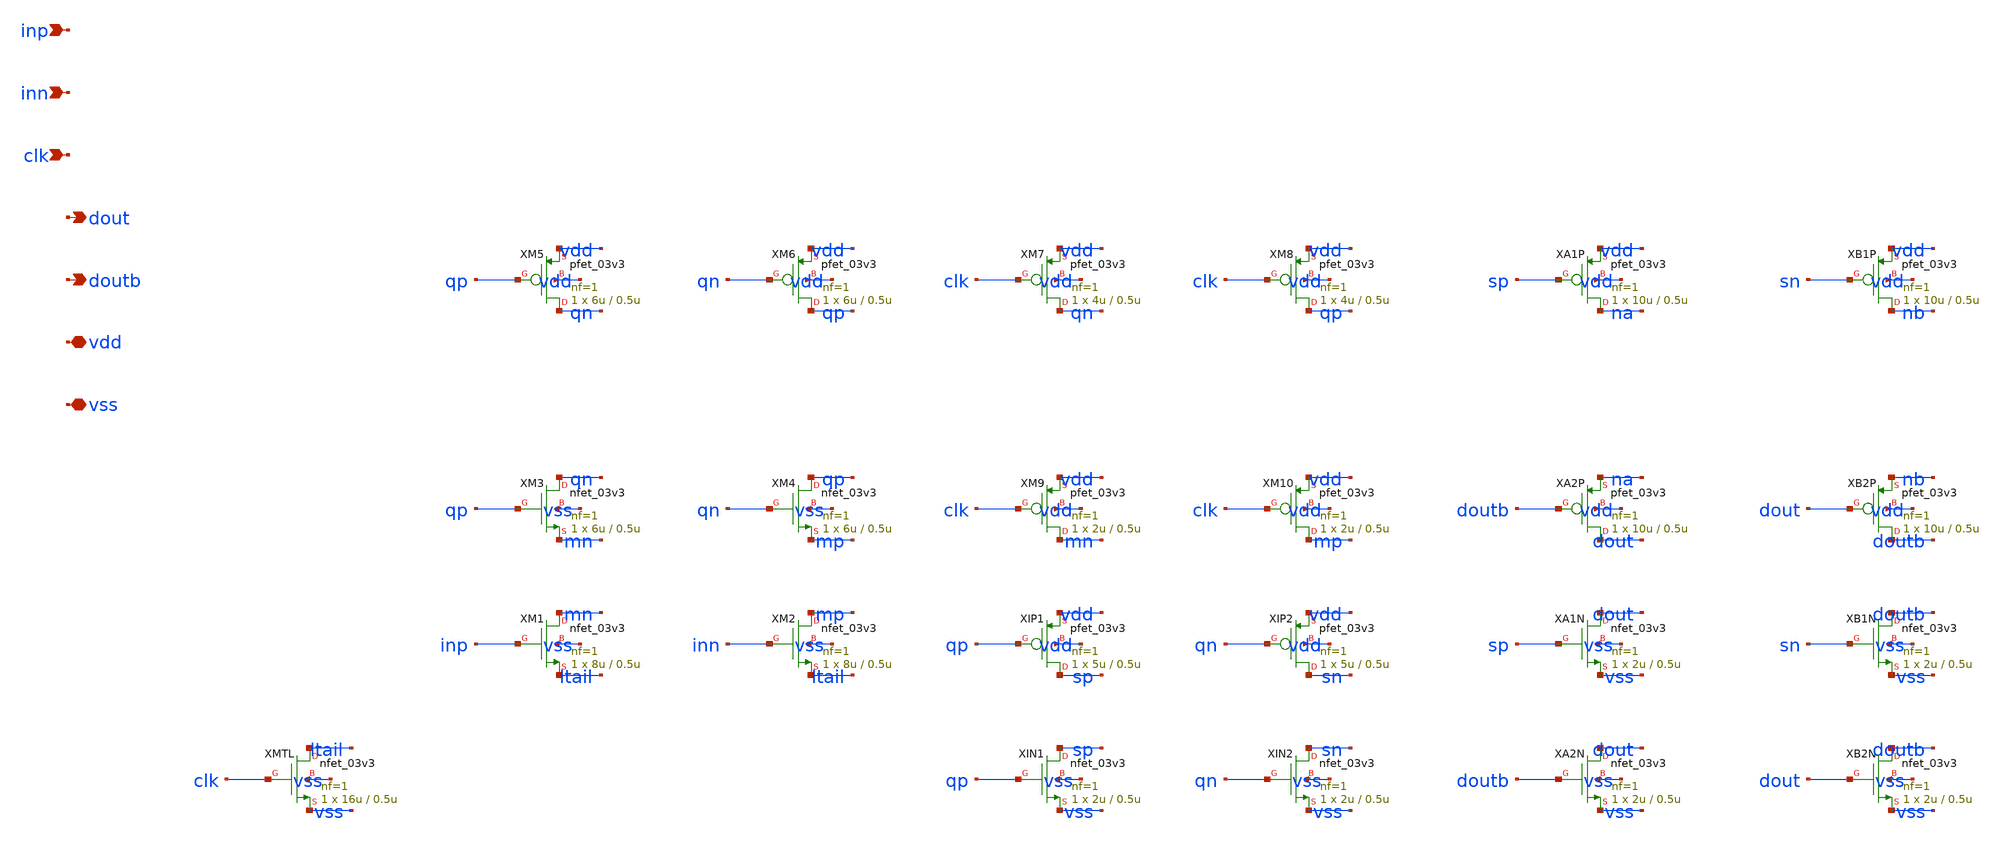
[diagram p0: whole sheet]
** sch_path: design/comparator_dut_latch.sch
**.subckt comparator_dut_latch inp inn clk dout doutb vdd vss
*.ipin inp
*.ipin inn
*.ipin clk
*.opin dout
*.opin doutb
*.iopin vdd
*.iopin vss
XMTL ltail clk vss vss nfet_03v3 L=0.5u W=16u nf=1 ad='int((nf+1)/2) * W/nf * 0.18u' as='int((nf+2)/2) * W/nf * 0.18u'
+ pd='2*int((nf+1)/2) * (W/nf + 0.18u)' ps='2*int((nf+2)/2) * (W/nf + 0.18u)' nrd='0.18u / W' nrs='0.18u / W'
+ sa=0 sb=0 sd=0 m=1
XM1 mn inp ltail vss nfet_03v3 L=0.5u W=8u nf=1 ad='int((nf+1)/2) * W/nf * 0.18u' as='int((nf+2)/2) * W/nf * 0.18u'
+ pd='2*int((nf+1)/2) * (W/nf + 0.18u)' ps='2*int((nf+2)/2) * (W/nf + 0.18u)' nrd='0.18u / W' nrs='0.18u / W'
+ sa=0 sb=0 sd=0 m=1
XM2 mp inn ltail vss nfet_03v3 L=0.5u W=8u nf=1 ad='int((nf+1)/2) * W/nf * 0.18u' as='int((nf+2)/2) * W/nf * 0.18u'
+ pd='2*int((nf+1)/2) * (W/nf + 0.18u)' ps='2*int((nf+2)/2) * (W/nf + 0.18u)' nrd='0.18u / W' nrs='0.18u / W'
+ sa=0 sb=0 sd=0 m=1
XM3 qn qp mn vss nfet_03v3 L=0.5u W=6u nf=1 ad='int((nf+1)/2) * W/nf * 0.18u' as='int((nf+2)/2) * W/nf * 0.18u'
+ pd='2*int((nf+1)/2) * (W/nf + 0.18u)' ps='2*int((nf+2)/2) * (W/nf + 0.18u)' nrd='0.18u / W' nrs='0.18u / W'
+ sa=0 sb=0 sd=0 m=1
XM4 qp qn mp vss nfet_03v3 L=0.5u W=6u nf=1 ad='int((nf+1)/2) * W/nf * 0.18u' as='int((nf+2)/2) * W/nf * 0.18u'
+ pd='2*int((nf+1)/2) * (W/nf + 0.18u)' ps='2*int((nf+2)/2) * (W/nf + 0.18u)' nrd='0.18u / W' nrs='0.18u / W'
+ sa=0 sb=0 sd=0 m=1
XM5 qn qp vdd vdd pfet_03v3 L=0.5u W=6u nf=1 ad='int((nf+1)/2) * W/nf * 0.18u' as='int((nf+2)/2) * W/nf * 0.18u'
+ pd='2*int((nf+1)/2) * (W/nf + 0.18u)' ps='2*int((nf+2)/2) * (W/nf + 0.18u)' nrd='0.18u / W' nrs='0.18u / W'
+ sa=0 sb=0 sd=0 m=1
XM6 qp qn vdd vdd pfet_03v3 L=0.5u W=6u nf=1 ad='int((nf+1)/2) * W/nf * 0.18u' as='int((nf+2)/2) * W/nf * 0.18u'
+ pd='2*int((nf+1)/2) * (W/nf + 0.18u)' ps='2*int((nf+2)/2) * (W/nf + 0.18u)' nrd='0.18u / W' nrs='0.18u / W'
+ sa=0 sb=0 sd=0 m=1
XM7 qn clk vdd vdd pfet_03v3 L=0.5u W=4u nf=1 ad='int((nf+1)/2) * W/nf * 0.18u' as='int((nf+2)/2) * W/nf * 0.18u'
+ pd='2*int((nf+1)/2) * (W/nf + 0.18u)' ps='2*int((nf+2)/2) * (W/nf + 0.18u)' nrd='0.18u / W' nrs='0.18u / W'
+ sa=0 sb=0 sd=0 m=1
XM8 qp clk vdd vdd pfet_03v3 L=0.5u W=4u nf=1 ad='int((nf+1)/2) * W/nf * 0.18u' as='int((nf+2)/2) * W/nf * 0.18u'
+ pd='2*int((nf+1)/2) * (W/nf + 0.18u)' ps='2*int((nf+2)/2) * (W/nf + 0.18u)' nrd='0.18u / W' nrs='0.18u / W'
+ sa=0 sb=0 sd=0 m=1
XM9 mn clk vdd vdd pfet_03v3 L=0.5u W=2u nf=1 ad='int((nf+1)/2) * W/nf * 0.18u' as='int((nf+2)/2) * W/nf * 0.18u'
+ pd='2*int((nf+1)/2) * (W/nf + 0.18u)' ps='2*int((nf+2)/2) * (W/nf + 0.18u)' nrd='0.18u / W' nrs='0.18u / W'
+ sa=0 sb=0 sd=0 m=1
XM10 mp clk vdd vdd pfet_03v3 L=0.5u W=2u nf=1 ad='int((nf+1)/2) * W/nf * 0.18u' as='int((nf+2)/2) * W/nf * 0.18u'
+ pd='2*int((nf+1)/2) * (W/nf + 0.18u)' ps='2*int((nf+2)/2) * (W/nf + 0.18u)' nrd='0.18u / W' nrs='0.18u / W'
+ sa=0 sb=0 sd=0 m=1
XIP1 sp qp vdd vdd pfet_03v3 L=0.5u W=5u nf=1 ad='int((nf+1)/2) * W/nf * 0.18u' as='int((nf+2)/2) * W/nf * 0.18u'
+ pd='2*int((nf+1)/2) * (W/nf + 0.18u)' ps='2*int((nf+2)/2) * (W/nf + 0.18u)' nrd='0.18u / W' nrs='0.18u / W'
+ sa=0 sb=0 sd=0 m=1
XIN1 sp qp vss vss nfet_03v3 L=0.5u W=2u nf=1 ad='int((nf+1)/2) * W/nf * 0.18u' as='int((nf+2)/2) * W/nf * 0.18u'
+ pd='2*int((nf+1)/2) * (W/nf + 0.18u)' ps='2*int((nf+2)/2) * (W/nf + 0.18u)' nrd='0.18u / W' nrs='0.18u / W'
+ sa=0 sb=0 sd=0 m=1
XIP2 sn qn vdd vdd pfet_03v3 L=0.5u W=5u nf=1 ad='int((nf+1)/2) * W/nf * 0.18u' as='int((nf+2)/2) * W/nf * 0.18u'
+ pd='2*int((nf+1)/2) * (W/nf + 0.18u)' ps='2*int((nf+2)/2) * (W/nf + 0.18u)' nrd='0.18u / W' nrs='0.18u / W'
+ sa=0 sb=0 sd=0 m=1
XIN2 sn qn vss vss nfet_03v3 L=0.5u W=2u nf=1 ad='int((nf+1)/2) * W/nf * 0.18u' as='int((nf+2)/2) * W/nf * 0.18u'
+ pd='2*int((nf+1)/2) * (W/nf + 0.18u)' ps='2*int((nf+2)/2) * (W/nf + 0.18u)' nrd='0.18u / W' nrs='0.18u / W'
+ sa=0 sb=0 sd=0 m=1
XA1P na sp vdd vdd pfet_03v3 L=0.5u W=10u nf=1 ad='int((nf+1)/2) * W/nf * 0.18u' as='int((nf+2)/2) * W/nf * 0.18u'
+ pd='2*int((nf+1)/2) * (W/nf + 0.18u)' ps='2*int((nf+2)/2) * (W/nf + 0.18u)' nrd='0.18u / W' nrs='0.18u / W'
+ sa=0 sb=0 sd=0 m=1
XA2P dout doutb na vdd pfet_03v3 L=0.5u W=10u nf=1 ad='int((nf+1)/2) * W/nf * 0.18u' as='int((nf+2)/2) * W/nf * 0.18u'
+ pd='2*int((nf+1)/2) * (W/nf + 0.18u)' ps='2*int((nf+2)/2) * (W/nf + 0.18u)' nrd='0.18u / W' nrs='0.18u / W'
+ sa=0 sb=0 sd=0 m=1
XA1N dout sp vss vss nfet_03v3 L=0.5u W=2u nf=1 ad='int((nf+1)/2) * W/nf * 0.18u' as='int((nf+2)/2) * W/nf * 0.18u'
+ pd='2*int((nf+1)/2) * (W/nf + 0.18u)' ps='2*int((nf+2)/2) * (W/nf + 0.18u)' nrd='0.18u / W' nrs='0.18u / W'
+ sa=0 sb=0 sd=0 m=1
XA2N dout doutb vss vss nfet_03v3 L=0.5u W=2u nf=1 ad='int((nf+1)/2) * W/nf * 0.18u' as='int((nf+2)/2) * W/nf * 0.18u'
+ pd='2*int((nf+1)/2) * (W/nf + 0.18u)' ps='2*int((nf+2)/2) * (W/nf + 0.18u)' nrd='0.18u / W' nrs='0.18u / W'
+ sa=0 sb=0 sd=0 m=1
XB1P nb sn vdd vdd pfet_03v3 L=0.5u W=10u nf=1 ad='int((nf+1)/2) * W/nf * 0.18u' as='int((nf+2)/2) * W/nf * 0.18u'
+ pd='2*int((nf+1)/2) * (W/nf + 0.18u)' ps='2*int((nf+2)/2) * (W/nf + 0.18u)' nrd='0.18u / W' nrs='0.18u / W'
+ sa=0 sb=0 sd=0 m=1
XB2P doutb dout nb vdd pfet_03v3 L=0.5u W=10u nf=1 ad='int((nf+1)/2) * W/nf * 0.18u' as='int((nf+2)/2) * W/nf * 0.18u'
+ pd='2*int((nf+1)/2) * (W/nf + 0.18u)' ps='2*int((nf+2)/2) * (W/nf + 0.18u)' nrd='0.18u / W' nrs='0.18u / W'
+ sa=0 sb=0 sd=0 m=1
XB1N doutb sn vss vss nfet_03v3 L=0.5u W=2u nf=1 ad='int((nf+1)/2) * W/nf * 0.18u' as='int((nf+2)/2) * W/nf * 0.18u'
+ pd='2*int((nf+1)/2) * (W/nf + 0.18u)' ps='2*int((nf+2)/2) * (W/nf + 0.18u)' nrd='0.18u / W' nrs='0.18u / W'
+ sa=0 sb=0 sd=0 m=1
XB2N doutb dout vss vss nfet_03v3 L=0.5u W=2u nf=1 ad='int((nf+1)/2) * W/nf * 0.18u' as='int((nf+2)/2) * W/nf * 0.18u'
+ pd='2*int((nf+1)/2) * (W/nf + 0.18u)' ps='2*int((nf+2)/2) * (W/nf + 0.18u)' nrd='0.18u / W' nrs='0.18u / W'
+ sa=0 sb=0 sd=0 m=1
**.ends
.end
